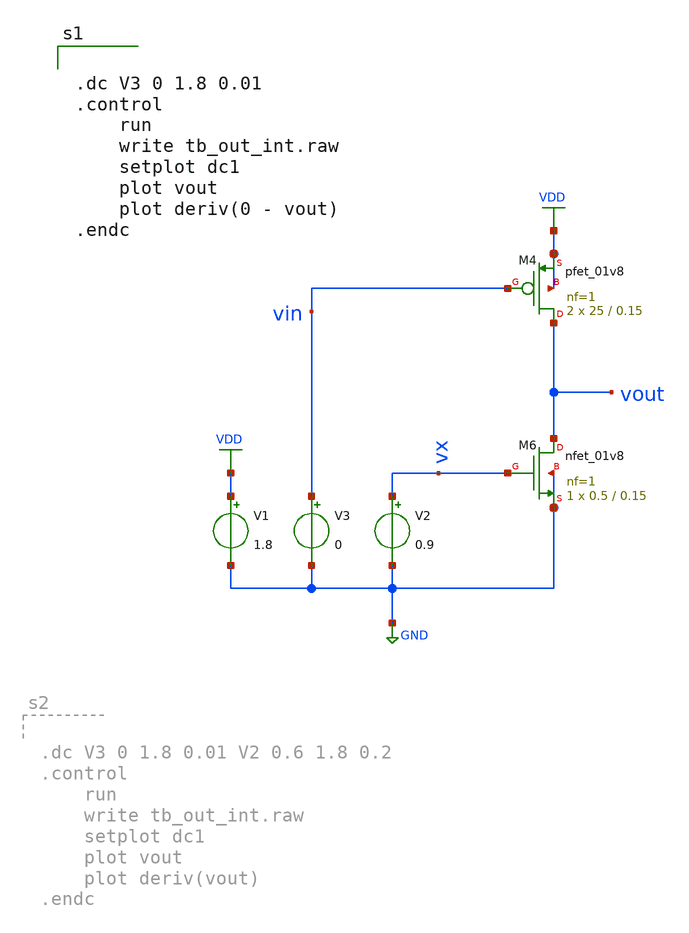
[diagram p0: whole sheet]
** sch_path: tb_out_int.sch
**.subckt tb_out_int
XM4 vout vin VDD VDD sky130_fd_pr__pfet_01v8 L=0.15 W=25 nf=1 ad='int((nf+1)/2) * W/nf * 0.29' as='int((nf+2)/2) * W/nf * 0.29'
+ pd='2*int((nf+1)/2) * (W/nf + 0.29)' ps='2*int((nf+2)/2) * (W/nf + 0.29)' nrd='0.29 / W' nrs='0.29 / W'
+ sa=0 sb=0 sd=0 mult=2 m=2
XM6 vout vx GND GND sky130_fd_pr__nfet_01v8 L=0.15 W=0.5 nf=1 ad='int((nf+1)/2) * W/nf * 0.29' as='int((nf+2)/2) * W/nf * 0.29'
+ pd='2*int((nf+1)/2) * (W/nf + 0.29)' ps='2*int((nf+2)/2) * (W/nf + 0.29)' nrd='0.29 / W' nrs='0.29 / W'
+ sa=0 sb=0 sd=0 mult=1 m=1
V1 VDD GND 1.8
V2 vx GND 0.9
V3 vin GND 0
**** begin user architecture code


.param mc_mm_switch=0
.param mc_pr_switch=0
.include /foss/pdks/sky130A/libs.tech/ngspice/corners/tt.spice
.include /foss/pdks/sky130A/libs.tech/ngspice/r+c/res_typical__cap_typical.spice
.include /foss/pdks/sky130A/libs.tech/ngspice/r+c/res_typical__cap_typical__lin.spice




.dc V3 0 1.8 0.01
.control
	run
	write tb_out_int.raw
	setplot dc1
	plot vout
	plot deriv(0 - vout)
.endc



**** end user architecture code
**.ends
.GLOBAL VDD
.GLOBAL GND
.end
